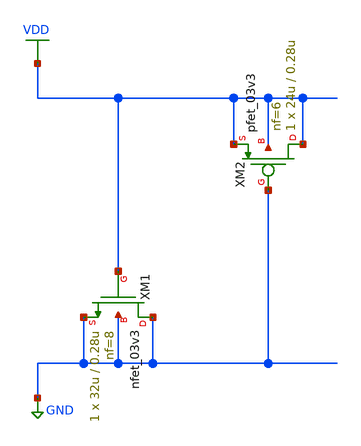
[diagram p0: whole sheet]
** sch_path: Schematic/break_before_make/decap_3.sch
**.subckt decap_3
XM1 GND VDD GND GND nfet_03v3 L=0.28u W=32u nf=8 ad='int((nf+1)/2) * W/nf * 0.18u' as='int((nf+2)/2) * W/nf * 0.18u'
+ pd='2*int((nf+1)/2) * (W/nf + 0.18u)' ps='2*int((nf+2)/2) * (W/nf + 0.18u)' nrd='0.18u / W' nrs='0.18u / W'
+ sa=0 sb=0 sd=0 m=1
XM2 VDD GND VDD VDD pfet_03v3 L=0.28u W=24u nf=6 ad='int((nf+1)/2) * W/nf * 0.18u' as='int((nf+2)/2) * W/nf * 0.18u'
+ pd='2*int((nf+1)/2) * (W/nf + 0.18u)' ps='2*int((nf+2)/2) * (W/nf + 0.18u)' nrd='0.18u / W' nrs='0.18u / W'
+ sa=0 sb=0 sd=0 m=1
**.ends
.GLOBAL VDD
.GLOBAL GND
.end
